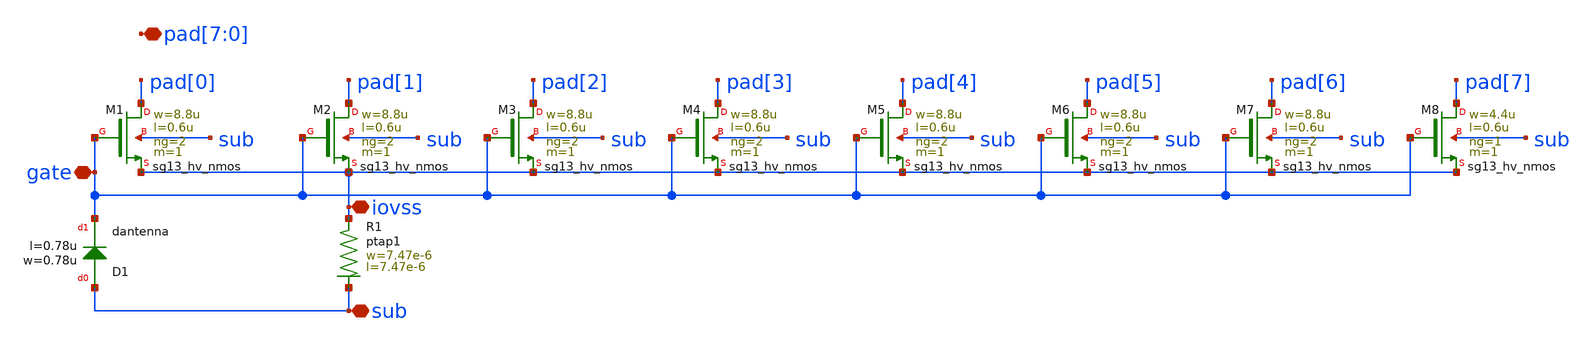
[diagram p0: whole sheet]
** sch_path: ihp-sg13cmos5l/libs.tech/xschem/hm_stdcells/sg13cmos5l_Clamp_N15N15D.sch
**.subckt sg13cmos5l_Clamp_N15N15D iovss gate
*+ pad[7],pad[6],pad[5],pad[4],pad[3],pad[2],pad[1],pad[0] sub
*.iopin iovss
*.iopin gate
*.iopin pad[7],pad[6],pad[5],pad[4],pad[3],pad[2],pad[1],pad[0]
*.iopin sub
XD1 sub gate dantenna l=0.78u w=0.78u
XM1 pad[0] gate iovss sub sg13_hv_nmos w=8.8u l=0.6u ng=2 m=1 mm_ok=1
XM2 pad[1] gate iovss sub sg13_hv_nmos w=8.8u l=0.6u ng=2 m=1 mm_ok=1
XM3 pad[2] gate iovss sub sg13_hv_nmos w=8.8u l=0.6u ng=2 m=1 mm_ok=1
XM4 pad[3] gate iovss sub sg13_hv_nmos w=8.8u l=0.6u ng=2 m=1 mm_ok=1
XM5 pad[4] gate iovss sub sg13_hv_nmos w=8.8u l=0.6u ng=2 m=1 mm_ok=1
XM6 pad[5] gate iovss sub sg13_hv_nmos w=8.8u l=0.6u ng=2 m=1 mm_ok=1
XM7 pad[6] gate iovss sub sg13_hv_nmos w=8.8u l=0.6u ng=2 m=1 mm_ok=1
XM8 pad[7] gate iovss sub sg13_hv_nmos w=4.4u l=0.6u ng=1 m=1 mm_ok=1
XR1 iovss sub ptap1 R=11.44 w=7.47e-6 l=7.47e-6
**.ends
.end
